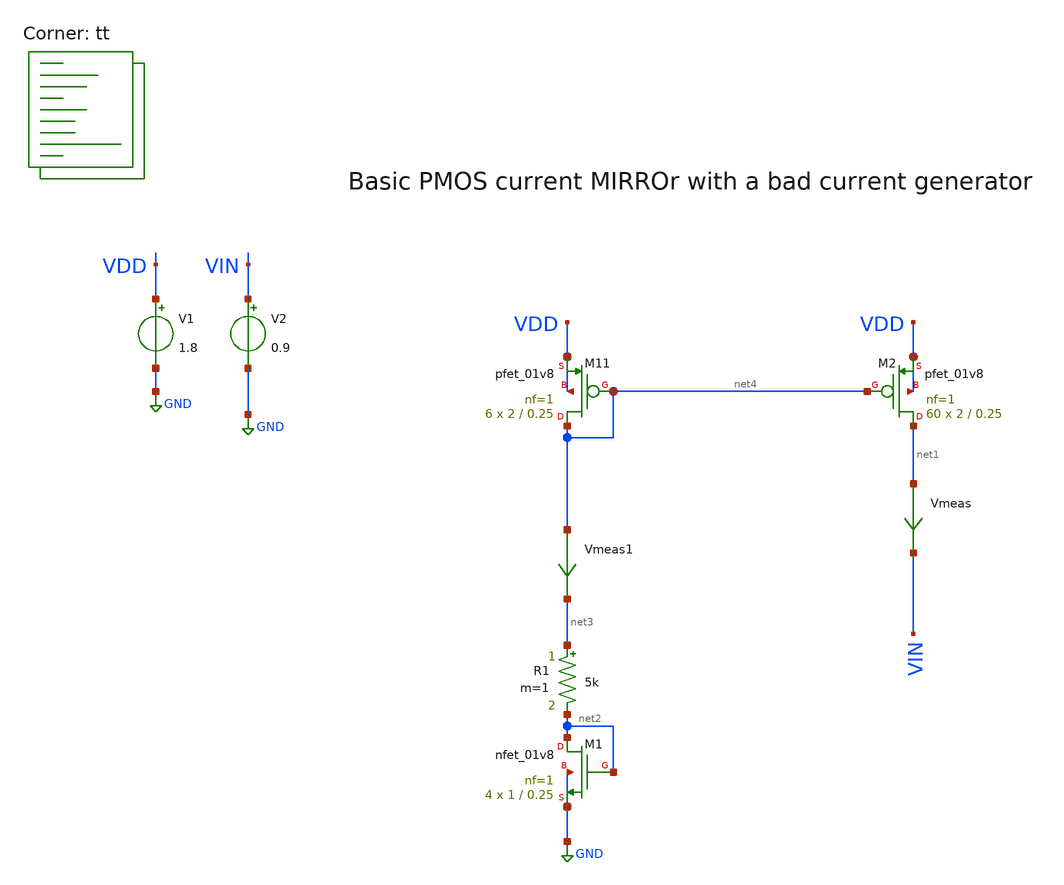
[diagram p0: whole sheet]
** sch_path: Analog_integrated_circuit_Design/chapter3/7/7.sch
**.subckt 7
V1 VDD GND 1.8
V2 VIN GND 0.9
Vmeas net1 VIN 0
.save i(vmeas)
XM1 net2 net2 GND GND sky130_fd_pr__nfet_01v8 L=0.25 W=1 nf=1 ad='int((1 + 1)/2) * 1 / 1 * 0.29' as='int((1 + 2)/2) * 1 / 1 * 0.29'
+ pd='2*int((1 + 1)/2) * (1 / 1 + 0.29)' ps='2*int((1 + 2)/2) * (1 / 1 + 0.29)' nrd='0.29 / 1 ' nrs='0.29 / 1 '
+ sa=0 sb=0 sd=0 mult=4 m=4
R1 net3 net2 5k m=1
Vmeas1 net4 net3 0
.save i(vmeas1)
XM11 net4 net4 VDD VDD sky130_fd_pr__pfet_01v8 L=0.25 W=2 nf=1 ad='int((nf+1)/2) * W/nf * 0.29' as='int((nf+2)/2) * W/nf * 0.29'
+ pd='2*int((nf+1)/2) * (W/nf + 0.29)' ps='2*int((nf+2)/2) * (W/nf + 0.29)' nrd='0.29 / W' nrs='0.29 / W'
+ sa=0 sb=0 sd=0 mult=6 m=6
XM2 net1 net4 VDD VDD sky130_fd_pr__pfet_01v8 L=0.25 W=2 nf=1 ad='int((nf+1)/2) * W/nf * 0.29' as='int((nf+2)/2) * W/nf * 0.29'
+ pd='2*int((nf+1)/2) * (W/nf + 0.29)' ps='2*int((nf+2)/2) * (W/nf + 0.29)' nrd='0.29 / W' nrs='0.29 / W'
+ sa=0 sb=0 sd=0 mult=60 m=60
**** begin user architecture code
.lib $::SKYWATER_MODELS/sky130.lib.spice tt

**************************************************************
**************************************************************
**************************************************************
**************************************************************
**************************************************************
*LIBs*********************************************************
**************************************************************
**************************************************************
**************************************************************
**************************************************************
**************************************************************
*.lib $::SKYWATER_MODELS/sky130.lib.spice tt
* chose the corners in the corner file
* tt_mm for mismatch
* ss ff sf fs standart corners
* ll hh lh hl capacitor and resistors corners
* mc for total process variation including corners
**************************************************************
**************************************************************
**************************************************************
**************************************************************
**************************************************************
*Corners/montecarlo options***********************************
**************************************************************
**************************************************************
**************************************************************
**************************************************************
**************************************************************
.TEMP 27
**************************************************************
**************************************************************
**************************************************************
**************************************************************
*SIMULATION and Plots*****************************************
**************************************************************
**************************************************************
**************************************************************
**************************************************************
.control
save all
dc V2 0 1.8 0.001
*dc simulation
plot i(Vmeas) i(Vmeas1)
plot v(VT) v(VT1)
plot 1/deriv(i(Vmeas))
.endc

**** end user architecture code
**.ends
.GLOBAL GND
.end
